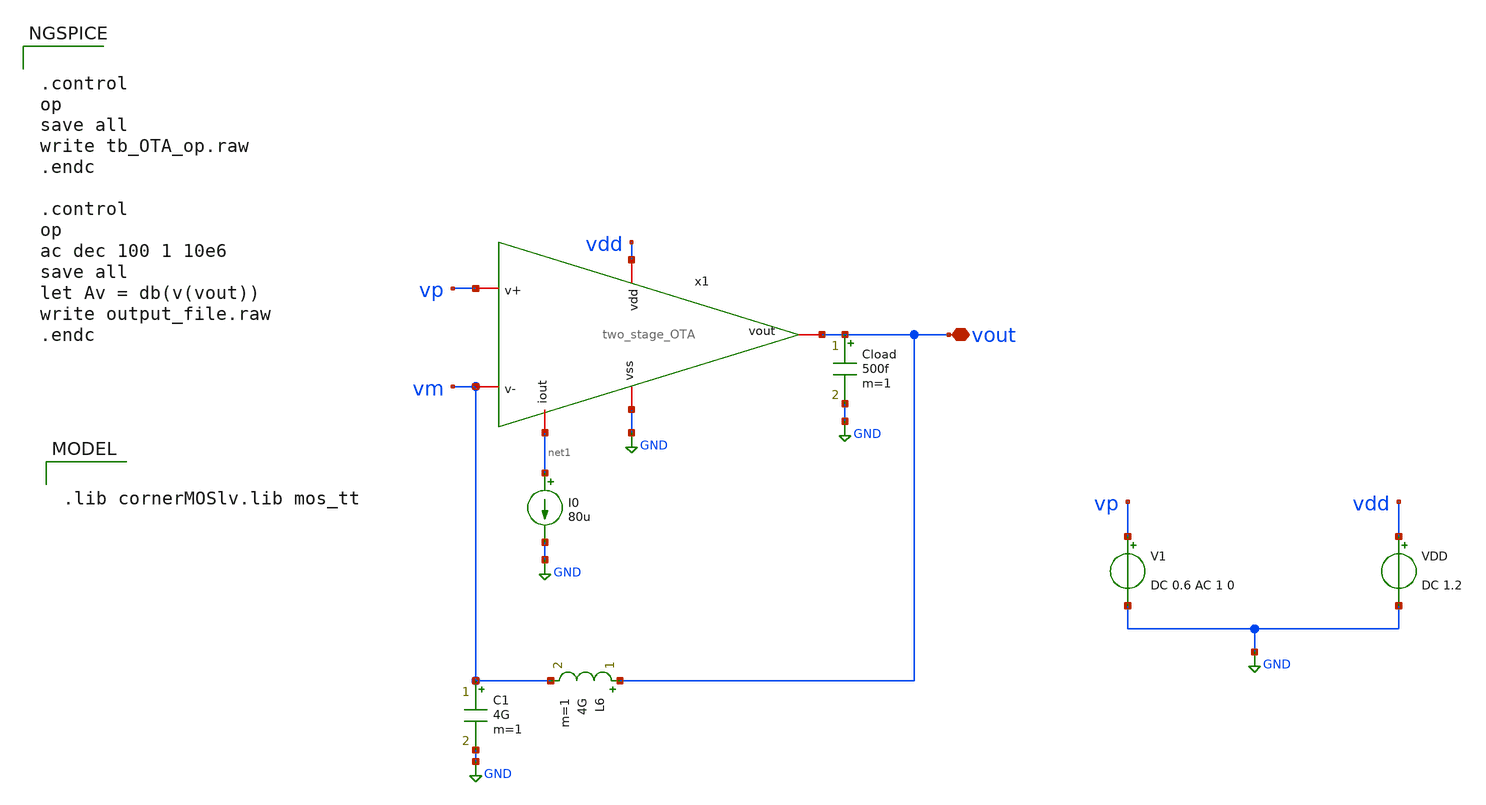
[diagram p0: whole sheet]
** sch_path: modules/module_1_bandgap_reference/part_1_OTA/gmid_example/testbenches/ota_testbench.sch
**.subckt ota_testbench vout
*.iopin vout
V1 vp GND DC 0.6 AC 1 0
VDD vdd GND DC 1.2
I0 net1 GND 80u
Cload vout GND 500f m=1
L6 vout vm 4G m=1
C1 vm GND 4G m=1
x1 vdd net1 vp vm vout GND two_stage_OTA
**** begin user architecture code

.lib cornerMOSlv.lib mos_tt



.control
op
save all
write tb_OTA_op.raw
.endc

.control
op
ac dec 100 1 10e6
save all
let Av = db(v(vout))
write output_file.raw
.endc


**** end user architecture code
**.ends

* expanding   symbol:  two_stage_OTA.sym # of pins=6
** sym_path: modules/module_1_bandgap_reference/part_1_OTA/gmid_example/schematic/two_stage_OTA.sym
** sch_path: modules/module_1_bandgap_reference/part_1_OTA/gmid_example/schematic/two_stage_OTA.sch
.subckt two_stage_OTA vdd iout v+ v- vout vss
*.iopin v-
*.iopin v+
*.iopin vss
*.iopin vdd
*.iopin iout
*.iopin vout
XM4 vout net1 vss vss sg13_lv_nmos w=3.09u l=6.24u ng=1 m=1 mm_ok=1
XM3 net1 net1 vss vss sg13_lv_nmos w=3.09u l=6.24u ng=1 m=1 mm_ok=1
XM1 net1 v+ net2 vdd sg13_lv_pmos w=2.75u l=5.46u ng=1 m=1 mm_ok=1
XM5 net2 iout vdd vdd sg13_lv_pmos w=66u l=9.98u ng=10 m=1 mm_ok=1
XM6 iout iout vdd vdd sg13_lv_pmos w=66u l=9.98u ng=10 m=1 mm_ok=1
XM2 vout v- net2 vdd sg13_lv_pmos w=2.75u l=5.46u ng=1 m=1 mm_ok=1
.ends

.GLOBAL GND
.end
